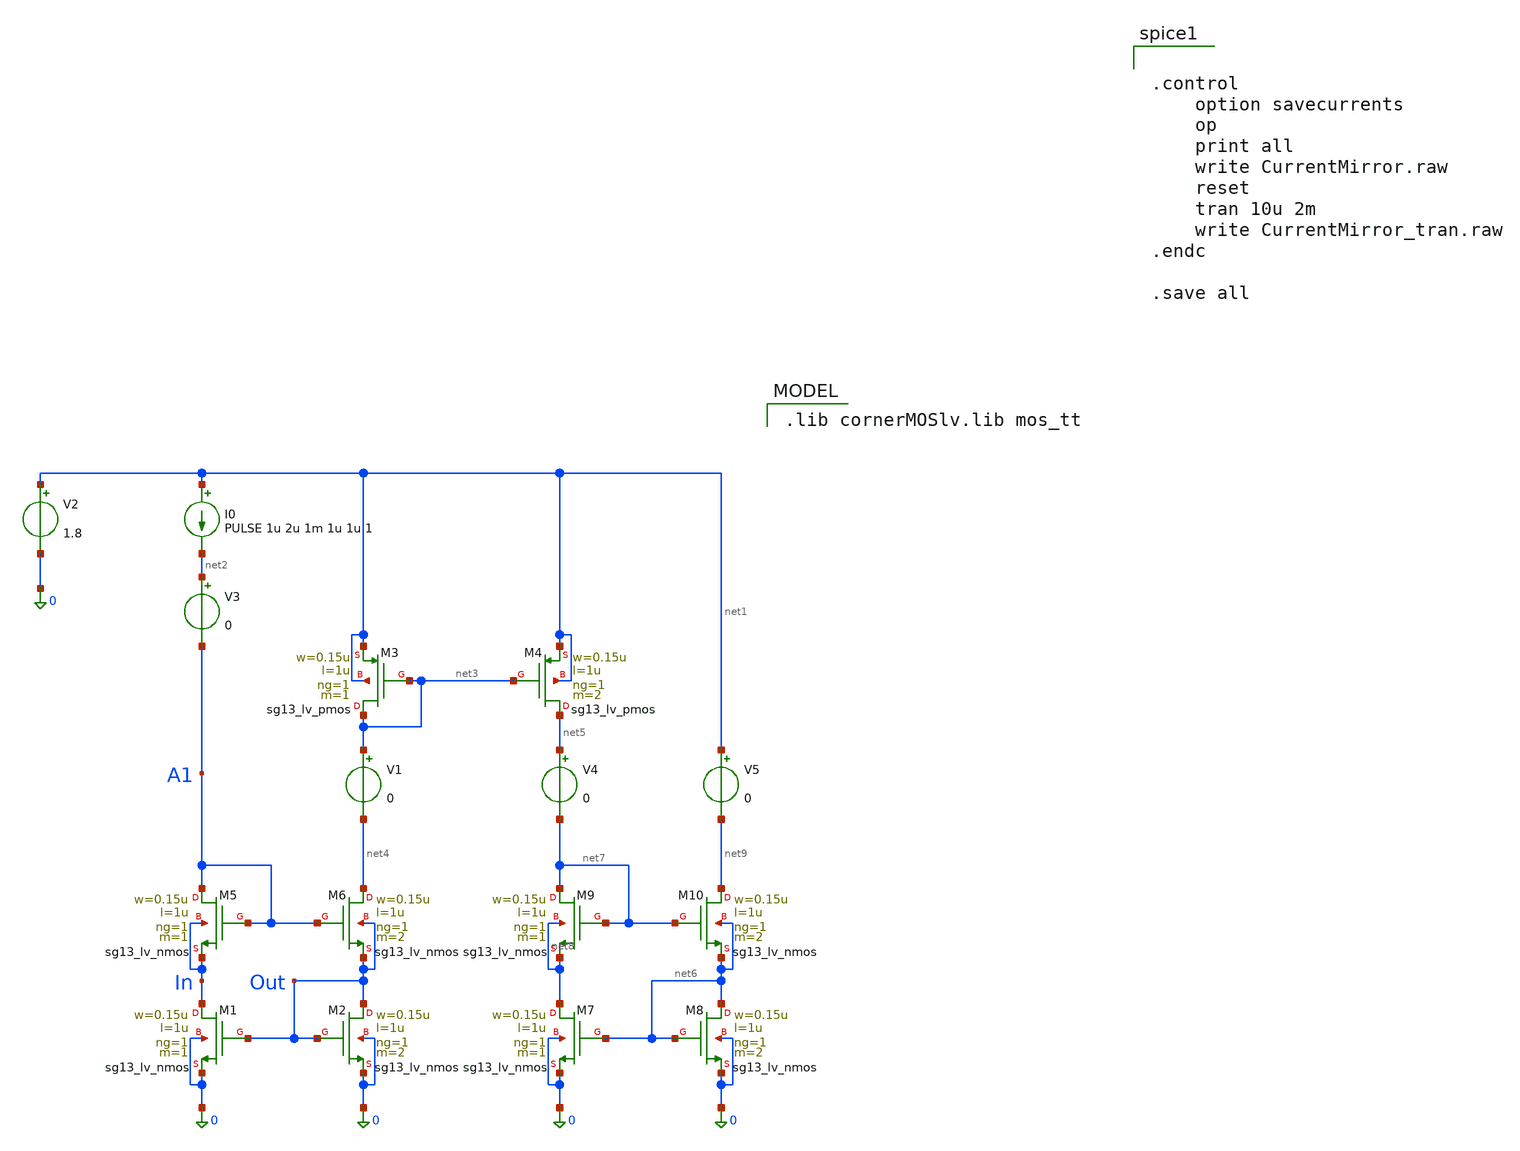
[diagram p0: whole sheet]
** sch_path: src/analog_mac/CurrentMirror2.sch
**.subckt CurrentMirror2
V1 net3 net4 0
V2 net1 0 1.8
I0 net1 net2 PULSE 1u 2u 1m 1u 1u 1
XM1 In Out 0 0 sg13_lv_nmos w=0.15u l=1u ng=1 m=1 mm_ok=1
XM2 Out Out 0 0 sg13_lv_nmos w=0.15u l=1u ng=1 m=2 mm_ok=1
V3 net2 A1 0
XM3 net3 net3 net1 net1 sg13_lv_pmos w=0.15u l=1u ng=1 m=1 mm_ok=1
XM4 net5 net3 net1 net1 sg13_lv_pmos w=0.15u l=1u ng=1 m=2 mm_ok=1
V4 net5 net7 0
XM5 A1 A1 In In sg13_lv_nmos w=0.15u l=1u ng=1 m=1 mm_ok=1
XM6 net4 A1 Out Out sg13_lv_nmos w=0.15u l=1u ng=1 m=2 mm_ok=1
XM7 net8 net6 0 0 sg13_lv_nmos w=0.15u l=1u ng=1 m=1 mm_ok=1
XM8 net6 net6 0 0 sg13_lv_nmos w=0.15u l=1u ng=1 m=2 mm_ok=1
XM9 net7 net7 net8 net8 sg13_lv_nmos w=0.15u l=1u ng=1 m=1 mm_ok=1
XM10 net9 net7 net6 net6 sg13_lv_nmos w=0.15u l=1u ng=1 m=2 mm_ok=1
V5 net1 net9 0
**** begin user architecture code
 .lib cornerMOSlv.lib mos_tt



.control
	option savecurrents
	op
	print all
	write CurrentMirror.raw
	reset
	tran 10u 2m
	write CurrentMirror_tran.raw
.endc

.save all


**** end user architecture code
**.ends
.end
